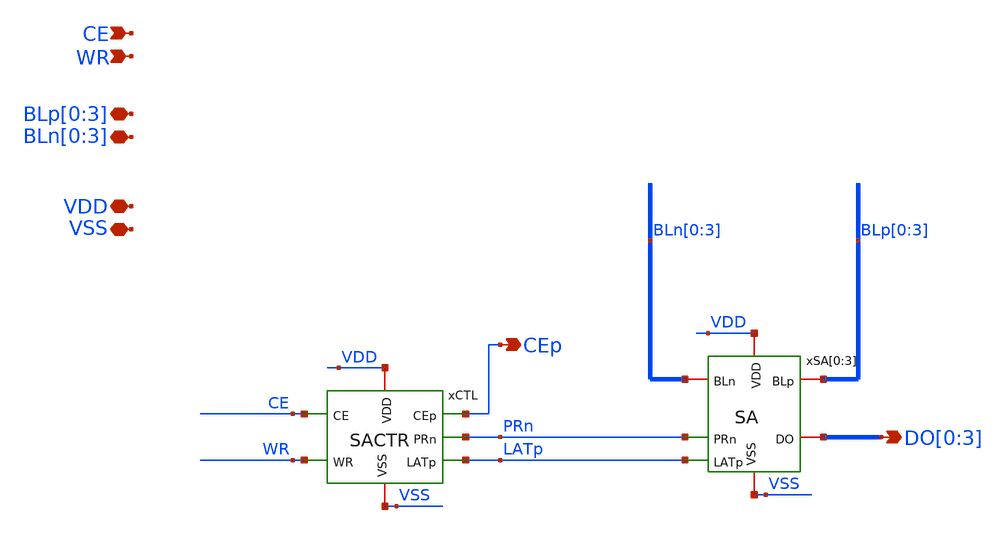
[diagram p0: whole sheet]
** sch_path: module/SRAM128/schematic/SRAM_SA4.sch
**.subckt SRAM_SA4 CE VSS VDD WR DO[0],DO[1],DO[2],DO[3] BLn[0],BLn[1],BLn[2],BLn[3]
*+ BLp[0],BLp[1],BLp[2],BLp[3] CEp
*.ipin CE
*.iopin VSS
*.iopin VDD
*.ipin WR
*.opin DO[0],DO[1],DO[2],DO[3]
*.iopin BLn[0],BLn[1],BLn[2],BLn[3]
*.iopin BLp[0],BLp[1],BLp[2],BLp[3]
*.opin CEp
xSA[0] VDD PRn DO[0] BLp[0] BLn[0] LATp VSS SA
xSA[1] VDD PRn DO[1] BLp[1] BLn[1] LATp VSS SA
xSA[2] VDD PRn DO[2] BLp[2] BLn[2] LATp VSS SA
xSA[3] VDD PRn DO[3] BLp[3] BLn[3] LATp VSS SA
xCTL PRn CE WR VDD VSS LATp CEp SACTR
**.ends

* expanding   symbol:  SA.sym # of pins=7
** sym_path: module/SRAM128/schematic/SA.sym
** sch_path: module/SRAM128/schematic/SA.sch
.subckt SA VDD PRn DO BLp BLn LATp VSS
*.iopin BLp
*.iopin BLn
*.ipin LATp
*.iopin VDD
*.iopin VSS
*.iopin DO
*.ipin PRn
XXM1 SENp BLn net3 VSS NMOS w=5.4u l=1u as=0 ad=0 ps=0 pd=0 nrd=0 nrs=0 m=1
XXM2 net1 SENp net2 VSS NMOS w=5.4u l=1u as=0 ad=0 ps=0 pd=0 nrd=0 nrs=0 m=1
XXM3 SENn LATp VDD VDD PMOS w=6.8u l=1u as=0 ad=0 ps=0 pd=0 nrd=0 nrs=0 m=1
XXM4 DO SENn VDD VDD PMOS w=10.8u l=1u as=0 ad=0 ps=0 pd=0 nrd=0 nrs=0 m=1
XXM5 SENn SENp VDD VDD PMOS w=3.4u l=1u as=0 ad=0 ps=0 pd=0 nrd=0 nrs=0 m=1
XXM6 net2 LATp VSS VSS NMOS w=10.8u l=1u as=0 ad=0 ps=0 pd=0 nrd=0 nrs=0 m=1
XXM7 SENn BLp net1 VSS NMOS w=5.4u l=1u as=0 ad=0 ps=0 pd=0 nrd=0 nrs=0 m=1
XXM8 net3 SENn net2 VSS NMOS w=5.4u l=1u as=0 ad=0 ps=0 pd=0 nrd=0 nrs=0 m=1
XXM9 SENp LATp VDD VDD PMOS w=6.8u l=1u as=0 ad=0 ps=0 pd=0 nrd=0 nrs=0 m=1
XXM11 SENp SENn VDD VDD PMOS w=3.4u l=1u as=0 ad=0 ps=0 pd=0 nrd=0 nrs=0 m=1
XXM12 DO SENn VSS VSS NMOS w=6.8u l=1u as=0 ad=0 ps=0 pd=0 nrd=0 nrs=0 m=1
XXM10 net4 SENp VDD VDD PMOS w=10.8u l=1u as=0 ad=0 ps=0 pd=0 nrd=0 nrs=0 m=1
XXM13 net4 SENp VSS VSS NMOS w=6.8u l=1u as=0 ad=0 ps=0 pd=0 nrd=0 nrs=0 m=1
XXM14 BLn PRn VDD VDD PMOS w=3.4u l=1.6u as=0 ad=0 ps=0 pd=0 nrd=0 nrs=0 m=1
XXM15 BLp PRn VDD VDD PMOS w=3.4u l=1.6u as=0 ad=0 ps=0 pd=0 nrd=0 nrs=0 m=1
XXM16 SENn SENp net2 VSS NMOS w=3.4u l=1u as=0 ad=0 ps=0 pd=0 nrd=0 nrs=0 m=1
XXM17 SENp SENn net2 VSS NMOS w=3.4u l=1u as=0 ad=0 ps=0 pd=0 nrd=0 nrs=0 m=1
.ends


* expanding   symbol:  SACTR.sym # of pins=7
** sym_path: module/SRAM128/schematic/SACTR.sym
** sch_path: module/SRAM128/schematic/SACTR.sch
.subckt SACTR PRn CE WR VDD VSS LATp CEp
*.opin PRn
*.ipin CE
*.iopin VDD
*.iopin VSS
*.opin LATp
*.ipin WR
*.opin CEp
XXM3 net1 CE VDD VDD PMOS w=3.4u l=1u as=0 ad=0 ps=0 pd=0 nrd=0 nrs=0 m=1
XXM7 net1 CE VSS VSS NMOS w=3.4u l=1u as=0 ad=0 ps=0 pd=0 nrd=0 nrs=0 m=1
XXM6 PRn net3 net2 VSS NMOS w=6.8u l=1u as=0 ad=0 ps=0 pd=0 nrd=0 nrs=0 m=1
XXM8 PRn net1 VDD VDD PMOS w=6.8u l=1u as=0 ad=0 ps=0 pd=0 nrd=0 nrs=0 m=1
XXM10 net2 net1 VSS VSS NMOS w=6.8u l=1u as=0 ad=0 ps=0 pd=0 nrd=0 nrs=0 m=1
XXM11 PRn net3 VDD VDD PMOS w=6.8u l=1u as=0 ad=0 ps=0 pd=0 nrd=0 nrs=0 m=1
XXM9 net3 PR_DLY VDD VDD PMOS w=3.4u l=2u as=0 ad=0 ps=0 pd=0 nrd=0 nrs=0 m=1
XXM12 net3 PR_DLY VSS VSS NMOS w=3.4u l=2u as=0 ad=0 ps=0 pd=0 nrd=0 nrs=0 m=1
XXM13 PR_DLY net1 VDD VDD PMOS w=3.4u l=1u as=0 ad=0 ps=0 pd=0 nrd=0 nrs=0 m=1
XXM14 PR_DLY net1 VSS VSS NMOS w=3.4u l=10u as=0 ad=0 ps=0 pd=0 nrd=0 nrs=0 m=1
XXM15 VDD PR_DLY VDD VDD PMOS w=3.4u l=6u as=0 ad=0 ps=0 pd=0 nrd=0 nrs=0 m=1
XXM1 LATp net5 net6 VSS NMOS w=6.8u l=1u as=0 ad=0 ps=0 pd=0 nrd=0 nrs=0 m=1
XXM4 LATp PRn VDD VDD PMOS w=6.8u l=1u as=0 ad=0 ps=0 pd=0 nrd=0 nrs=0 m=1
XXM16 net6 PRn VSS VSS NMOS w=6.8u l=1u as=0 ad=0 ps=0 pd=0 nrd=0 nrs=0 m=1
XXM21 net4 LAT_DLY VDD VDD PMOS w=3.4u l=2u as=0 ad=0 ps=0 pd=0 nrd=0 nrs=0 m=1
XXM22 net4 LAT_DLY VSS VSS NMOS w=3.4u l=2u as=0 ad=0 ps=0 pd=0 nrd=0 nrs=0 m=1
XXM23 LAT_DLY PRn VDD VDD PMOS w=3.4u l=1u as=0 ad=0 ps=0 pd=0 nrd=0 nrs=0 m=1
XXM24 LAT_DLY PRn VSS VSS NMOS w=3.4u l=10u as=0 ad=0 ps=0 pd=0 nrd=0 nrs=0 m=1
XXM25 VDD LAT_DLY VDD VDD PMOS w=3.4u l=4.2u as=0 ad=0 ps=0 pd=0 nrd=0 nrs=0 m=1
XXM27 net5 WR net7 VDD PMOS w=3.4u l=1u as=0 ad=0 ps=0 pd=0 nrd=0 nrs=0 m=1
XXM28 net5 net4 VSS VSS NMOS w=3.4u l=1u as=0 ad=0 ps=0 pd=0 nrd=0 nrs=0 m=1
XXM17 net7 net4 VDD VDD PMOS w=3.4u l=1u as=0 ad=0 ps=0 pd=0 nrd=0 nrs=0 m=1
XXM18 net5 WR VSS VSS NMOS w=3.4u l=1u as=0 ad=0 ps=0 pd=0 nrd=0 nrs=0 m=1
XXM5 LATp net5 VDD VDD PMOS w=6.8u l=1u as=0 ad=0 ps=0 pd=0 nrd=0 nrs=0 m=1
XXM2 CEp net1 VDD VDD PMOS w=3.4u l=1u as=0 ad=0 ps=0 pd=0 nrd=0 nrs=0 m=1
XXM19 CEp net1 VSS VSS NMOS w=3.4u l=1u as=0 ad=0 ps=0 pd=0 nrd=0 nrs=0 m=1
.ends

.end
